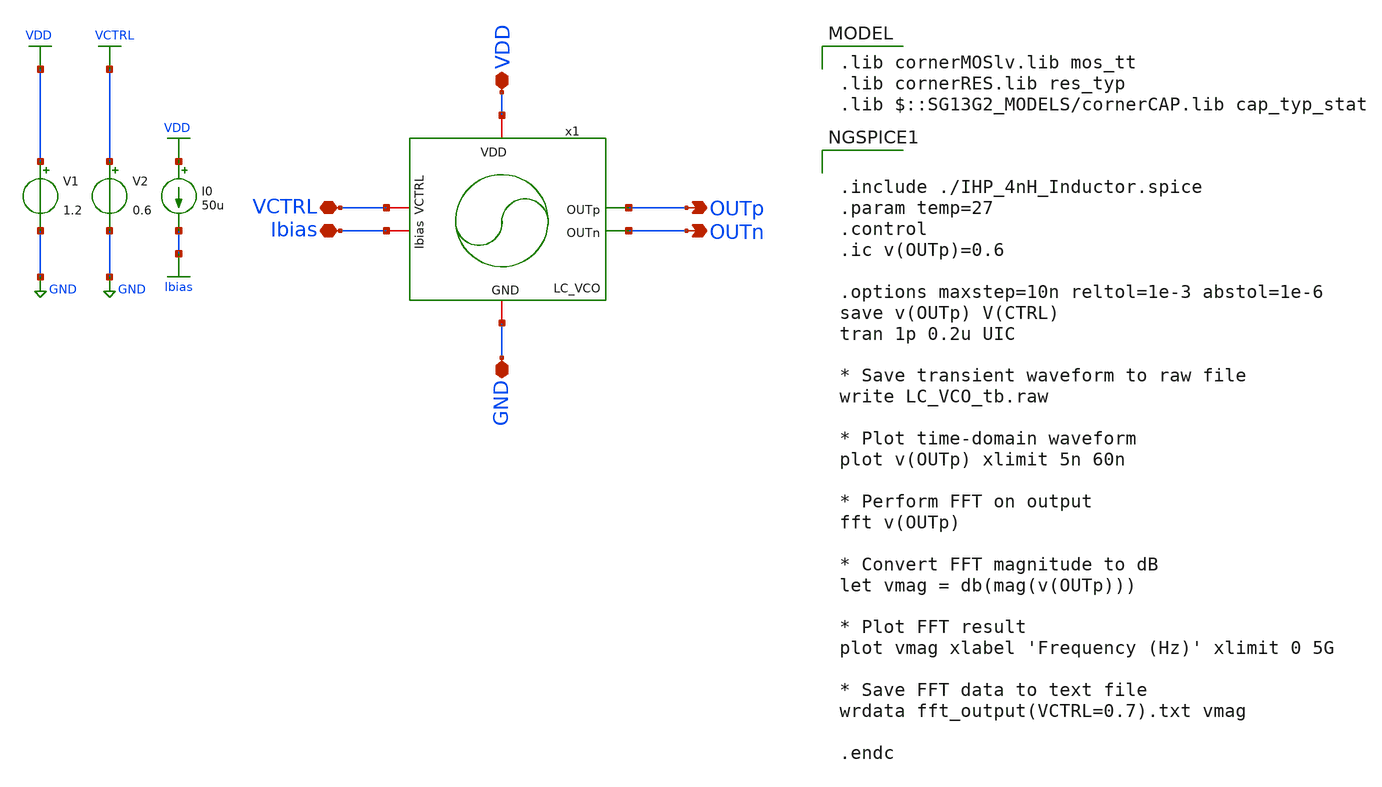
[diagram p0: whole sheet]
** sch_path: schematic/blocks/top-pll/lc-vco/LC_VCO_tb.sch
**.subckt LC_VCO_tb OUTp OUTn VDD VCTRL GND Ibias
*.opin OUTp
*.opin OUTn
*.iopin VDD
*.iopin VCTRL
*.iopin GND
*.iopin Ibias
V1 VDD GND 1.2
V2 VCTRL GND 0.6
I0 VDD Ibias 50u
x1 VDD OUTp OUTn Ibias VCTRL GND LC_VCO
**** begin user architecture code
 .lib cornerMOSlv.lib mos_tt
.lib cornerRES.lib res_typ
.lib $::SG13G2_MODELS/cornerCAP.lib cap_typ_stat



.include ./IHP_4nH_Inductor.spice
.param temp=27
.control
.ic v(OUTp)=0.6

.options maxstep=10n reltol=1e-3 abstol=1e-6
save v(OUTp) V(CTRL)
tran 1p 0.2u UIC

* Save transient waveform to raw file
write LC_VCO_tb.raw

* Plot time-domain waveform
plot v(OUTp) xlimit 5n 60n

* Perform FFT on output
fft v(OUTp)

* Convert FFT magnitude to dB
let vmag = db(mag(v(OUTp)))

* Plot FFT result
plot vmag xlabel 'Frequency (Hz)' xlimit 0 5G

* Save FFT data to text file
wrdata fft_output(VCTRL=0.7).txt vmag

.endc


**** end user architecture code
**.ends
.GLOBAL GND
.GLOBAL VDD
.GLOBAL VCTRL
.GLOBAL Ibias
.end
